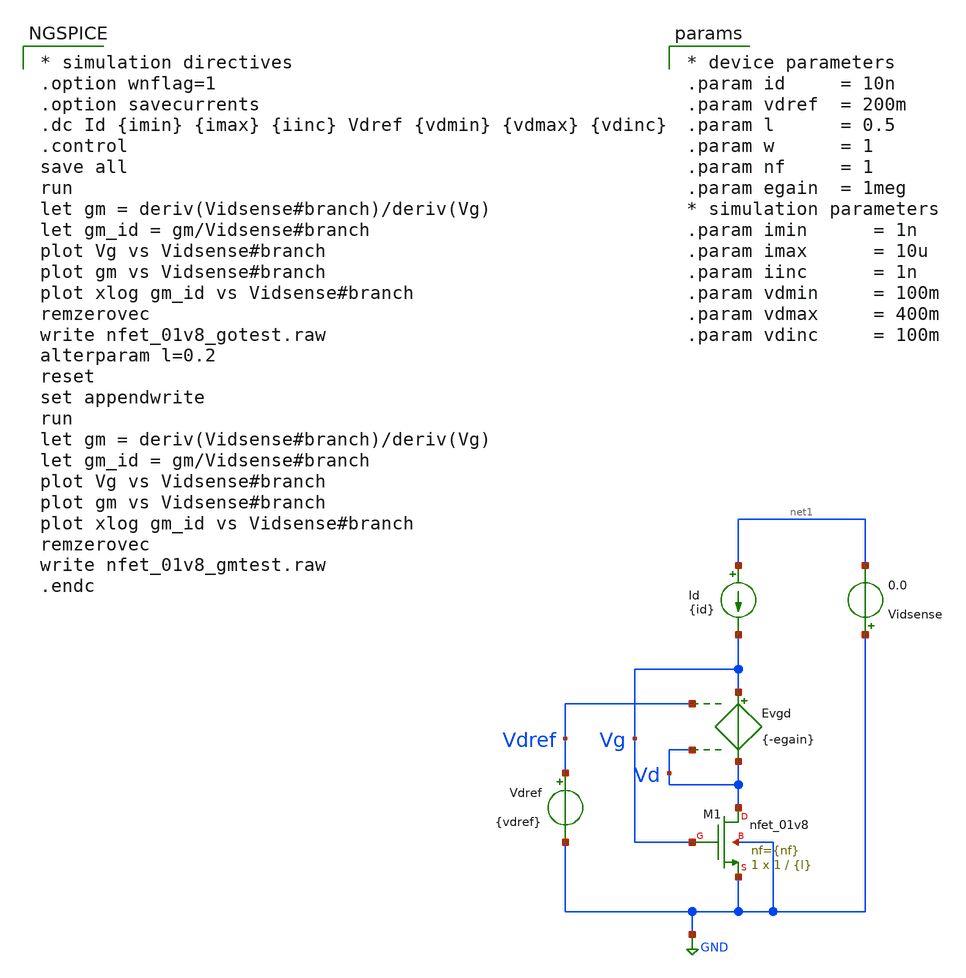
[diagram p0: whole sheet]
** sch_path: cace/tb_nfet_01v8_gmtest.sch
**.subckt tb_nfet_01v8_gmtest
Evgd Vg Vd Vdref Vd {-egain}
Id net1 Vg {id}
Vdref Vdref GND {vdref}
Vidsense GND net1 0.0
XM1 Vd Vg GND GND sky130_fd_pr__nfet_01v8 L={l} W=1 nf={nf} ad='int((nf+1)/2) * W/nf * 0.29' as='int((nf+2)/2) * W/nf * 0.29'
+ pd='2*int((nf+1)/2) * (W/nf + 0.29)' ps='2*int((nf+2)/2) * (W/nf + 0.29)' nrd='0.29 / W' nrs='0.29 / W'
+ sa=0 sb=0 sd=0 mult=1 m=1
**** begin user architecture code

** opencircuitdesign pdks install
.lib $::SKYWATER_MODELS/sky130.lib.spice tt



* simulation directives
.option wnflag=1
.option savecurrents
.dc Id {imin} {imax} {iinc} Vdref {vdmin} {vdmax} {vdinc}
.control
save all
run
let gm = deriv(Vidsense#branch)/deriv(Vg)
let gm_id = gm/Vidsense#branch
plot Vg vs Vidsense#branch
plot gm vs Vidsense#branch
plot xlog gm_id vs Vidsense#branch
remzerovec
write nfet_01v8_gotest.raw
alterparam l=0.2
reset
set appendwrite
run
let gm = deriv(Vidsense#branch)/deriv(Vg)
let gm_id = gm/Vidsense#branch
plot Vg vs Vidsense#branch
plot gm vs Vidsense#branch
plot xlog gm_id vs Vidsense#branch
remzerovec
write nfet_01v8_gmtest.raw
.endc



* device parameters
.param id     = 10n
.param vdref  = 200m
.param l      = 0.5
.param w      = 1
.param nf     = 1
.param egain  = 1meg
* simulation parameters
.param imin      = 1n
.param imax      = 10u
.param iinc      = 1n
.param vdmin     = 100m
.param vdmax     = 400m
.param vdinc     = 100m


**** end user architecture code
**.ends
.GLOBAL GND
.end
